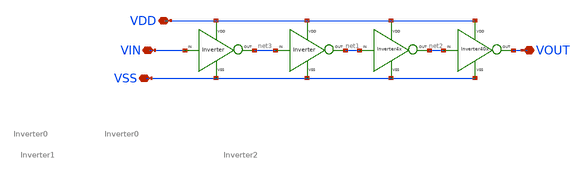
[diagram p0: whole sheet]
** sch_path: xschem/DC_DC_Converter_xschem/OTHERS/DC_DC_Converter_JV11/BUFFER/BUFFER_NMOS/BUFFER_N.sch
**.subckt BUFFER_N VDD VIN VSS VOUT
*.iopin VDD
*.iopin VIN
*.iopin VSS
*.iopin VOUT
X7 net3 net1 VDD VSS Inverter0
X8 net1 net2 VDD VSS Inverter1
X79 net2 VOUT VDD VSS Inverter2
X29 VIN net3 VDD VSS Inverter0
**.ends
.end
